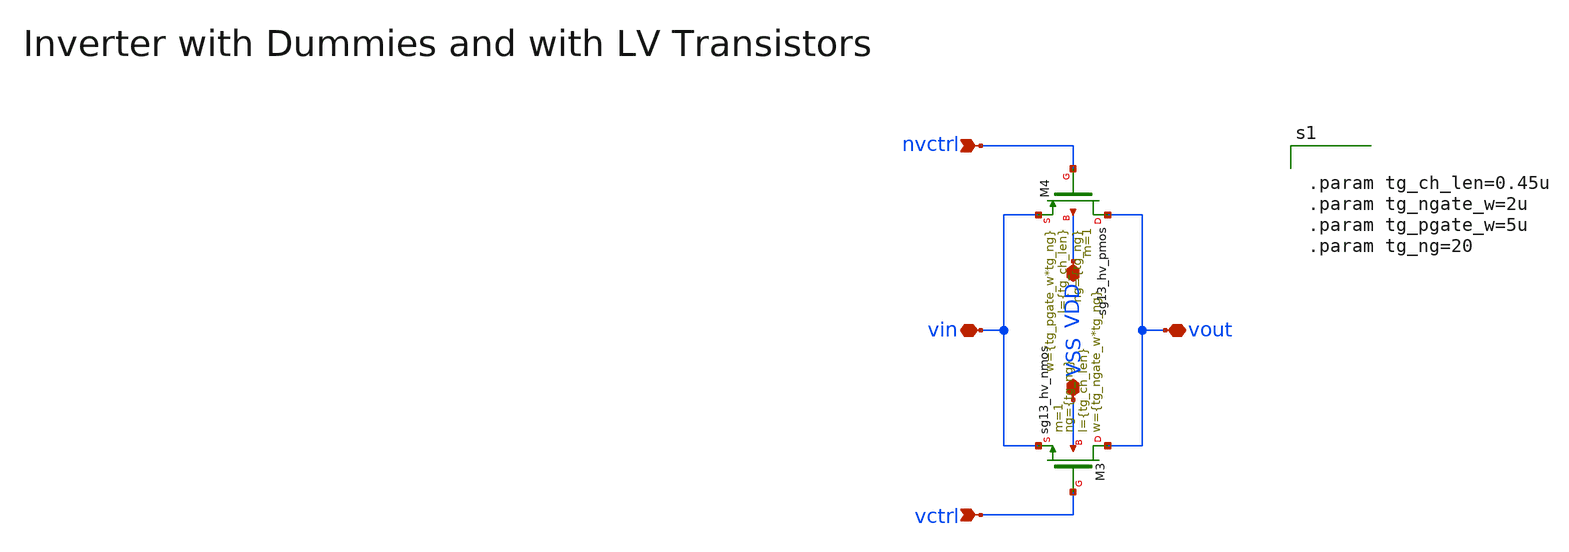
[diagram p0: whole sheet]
** sch_path: macros/heichips26_vcr/macros/switched_capacitor/schematic/xschem/transmission_gate.sch
**.subckt transmission_gate vin vout vctrl nvctrl VDD VSS
*.iopin vin
*.iopin vout
*.ipin vctrl
*.ipin nvctrl
*.iopin VDD
*.iopin VSS
XM3 vout vctrl vin VSS sg13_hv_nmos w={tg_ngate_w*tg_ng} l={tg_ch_len} ng={tg_ng} m=1 mm_ok=1
XM4 vout nvctrl vin VDD sg13_hv_pmos w={tg_pgate_w*tg_ng} l={tg_ch_len} ng={tg_ng} m=1 mm_ok=1
**** begin user architecture code


.param tg_ch_len=0.45u
.param tg_ngate_w=2u
.param tg_pgate_w=5u
.param tg_ng=20


**** end user architecture code
**.ends
.end
